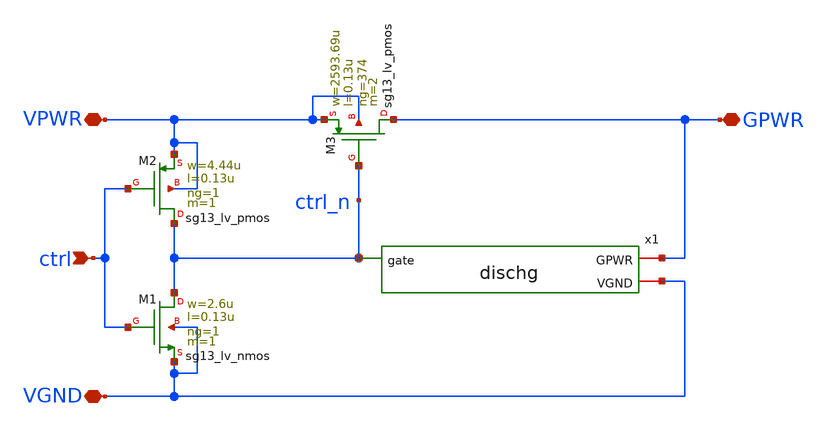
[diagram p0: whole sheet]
** sch_path: ihp-sg13cmos5l/libs.tech/xschem/hm_analog/hm_pg_lv_17x200.sch
**.subckt hm_pg_lv_17x200 ctrl VPWR VGND GPWR
*.ipin ctrl
*.iopin VPWR
*.iopin VGND
*.iopin GPWR
XM1 ctrl_n ctrl VGND VGND sg13_lv_nmos w=2.6u l=0.13u ng=1 m=1 mm_ok=1
XM2 ctrl_n ctrl VPWR VPWR sg13_lv_pmos w=4.44u l=0.13u ng=1 m=1 mm_ok=1
XM3 GPWR ctrl_n VPWR VPWR sg13_lv_pmos w=2593.69u l=0.13u ng=374 m=2 mm_ok=1
x1 VGND GPWR ctrl_n dischg
**.ends

* expanding   symbol:  hm_analog/dischg.sym # of pins=3
** sym_path: ihp-sg13cmos5l/libs.tech/xschem/hm_analog/dischg.sym
** sch_path: ihp-sg13cmos5l/libs.tech/xschem/hm_analog/dischg.sch
.subckt dischg VGND GPWR gate
*.iopin GPWR
*.iopin VGND
*.ipin gate
XM1 GPWR gate net2 VGND sg13_lv_nmos w=4u l=0.65u ng=1 m=1 mm_ok=1
XM2 net2 gate net3 VGND sg13_lv_nmos w=4u l=0.65u ng=1 m=1 mm_ok=1
XM3 net3 gate net4 VGND sg13_lv_nmos w=4u l=0.65u ng=1 m=1 mm_ok=1
XM4 net4 gate net1 VGND sg13_lv_nmos w=4u l=0.65u ng=1 m=1 mm_ok=1
XM5 net1 gate net7 VGND sg13_lv_nmos w=4u l=0.65u ng=1 m=1 mm_ok=1
XM6 net7 gate net6 VGND sg13_lv_nmos w=4u l=0.65u ng=1 m=1 mm_ok=1
XM7 net6 gate net5 VGND sg13_lv_nmos w=4u l=0.65u ng=1 m=1 mm_ok=1
XM8 net5 gate VGND VGND sg13_lv_nmos w=4u l=0.65u ng=1 m=1 mm_ok=1
XM9 GPWR gate net9 VGND sg13_lv_nmos w=4u l=0.65u ng=1 m=1 mm_ok=1
XM10 net9 gate net10 VGND sg13_lv_nmos w=4u l=0.65u ng=1 m=1 mm_ok=1
XM11 net10 gate net11 VGND sg13_lv_nmos w=4u l=0.65u ng=1 m=1 mm_ok=1
XM12 net11 gate net8 VGND sg13_lv_nmos w=4u l=0.65u ng=1 m=1 mm_ok=1
XM13 net8 gate net14 VGND sg13_lv_nmos w=4u l=0.65u ng=1 m=1 mm_ok=1
XM14 net14 gate net13 VGND sg13_lv_nmos w=4u l=0.65u ng=1 m=1 mm_ok=1
XM15 net13 gate net12 VGND sg13_lv_nmos w=4u l=0.65u ng=1 m=1 mm_ok=1
XM16 net12 gate VGND VGND sg13_lv_nmos w=4u l=0.65u ng=1 m=1 mm_ok=1
.ends

.end
